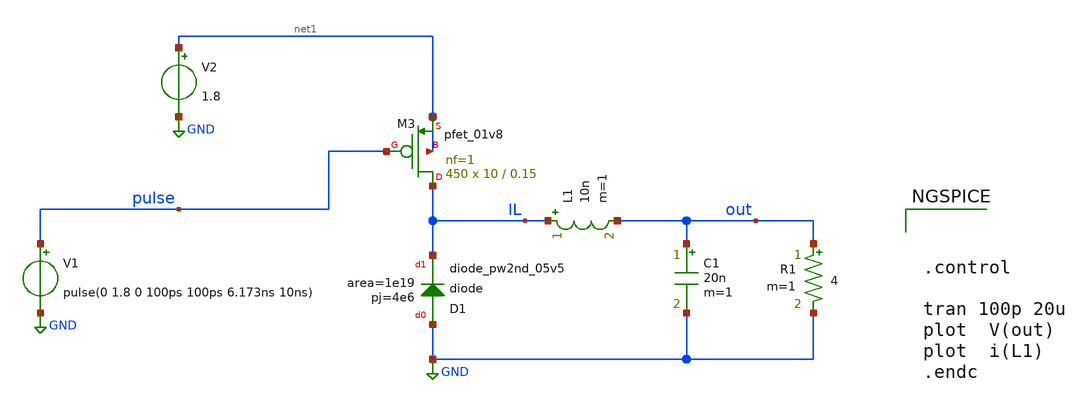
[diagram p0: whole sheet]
** sch_path: xschem/DC_DC_Converter_xschem/OTHERS/DC_DC_Converter_5/TOP_LEVEL/buck_asynchronous.sch
**.subckt buck_asynchronous
XM3 IL pulse net1 net1 sky130_fd_pr__pfet_01v8 L=0.15 W=10 nf=1 ad='int((nf+1)/2) * W/nf * 0.29' as='int((nf+2)/2) * W/nf * 0.29'
+ pd='2*int((nf+1)/2) * (W/nf + 0.29)' ps='2*int((nf+2)/2) * (W/nf + 0.29)' nrd='0.29 / W' nrs='0.29 / W'
+ sa=0 sb=0 sd=0 mult=450 m=450
V2 net1 GND 1.8
L1 IL out 10n m=1
C1 out GND 20n m=1
R1 out GND 4 m=1
V1 pulse GND pulse(0 1.8 0 100ps 100ps 6.173ns 10ns)
XD1 GND IL sky130_fd_pr__diode_pw2nd_05v5 area=1e19 pj=4e6
**** begin user architecture code

** opencircuitdesign pdks install
.lib $::SKYWATER_MODELS/sky130.lib.spice tt





.control

tran 100p 20u
plot  V(out)
plot  i(L1)
.endc


**** end user architecture code
**.ends
.GLOBAL GND
.end
